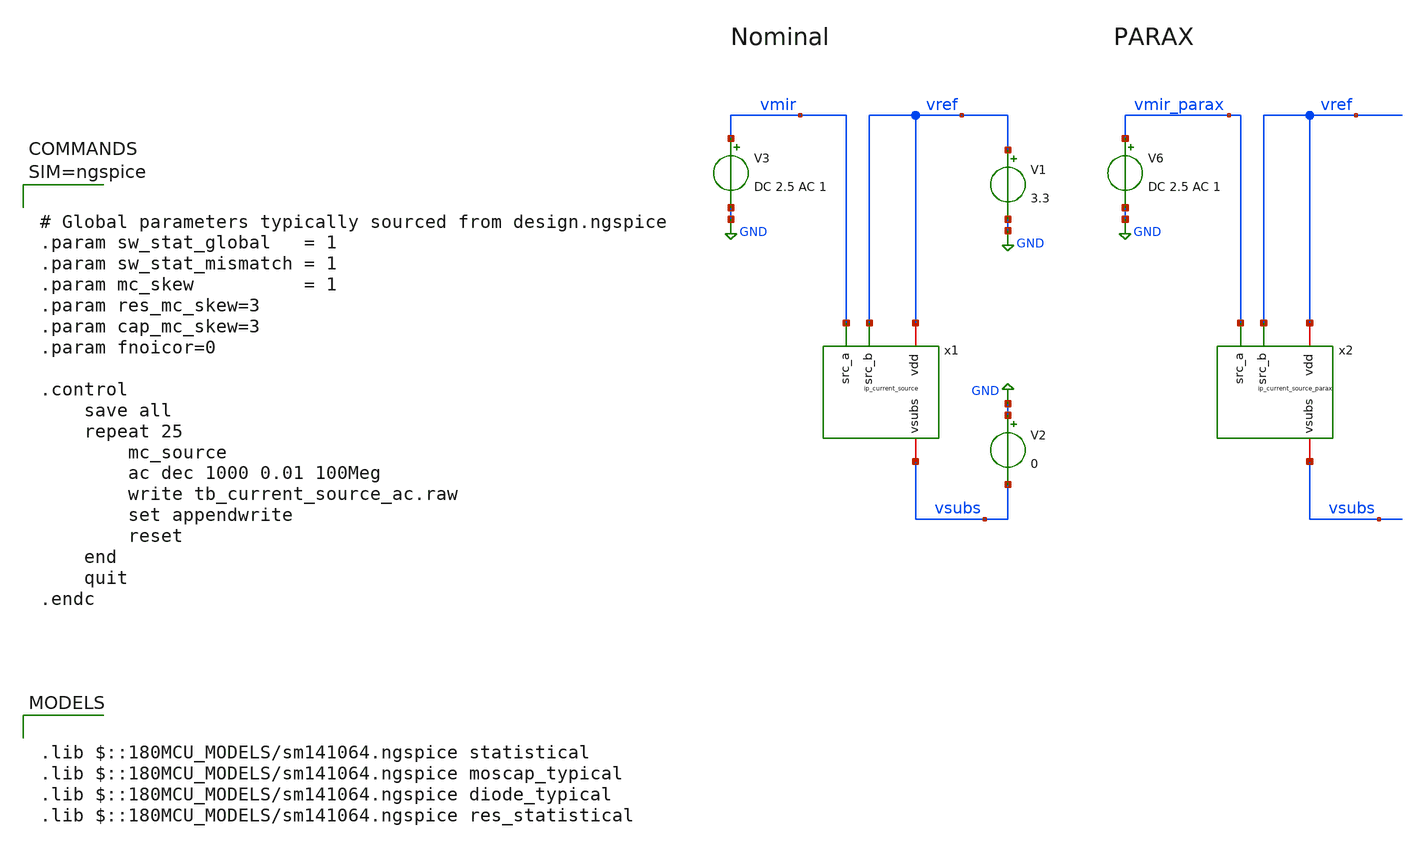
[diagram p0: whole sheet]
** sch_path: xschem/tb_current_source_ac.sch
**.subckt tb_current_source_ac
x1 vref vmir vsubs vref ip_current_source
V1 vref GND 3.3
V2 GND vsubs 0
V3 vmir GND DC 2.5 AC 1
x2 vref vmir_parax vsubs vref ip_current_source_parax
V6 vmir_parax GND DC 2.5 AC 1
**** begin user architecture code

.lib $::180MCU_MODELS/sm141064.ngspice statistical
.lib $::180MCU_MODELS/sm141064.ngspice moscap_typical
.lib $::180MCU_MODELS/sm141064.ngspice diode_typical
.lib $::180MCU_MODELS/sm141064.ngspice res_statistical




# Global parameters typically sourced from design.ngspice
.param sw_stat_global   = 1
.param sw_stat_mismatch = 1
.param mc_skew          = 1
.param res_mc_skew=3
.param cap_mc_skew=3
.param fnoicor=0

.control
	save all
	repeat 25
		mc_source
		ac dec 1000 0.01 100Meg
		write tb_current_source_ac.raw
		set appendwrite
		reset
	end
	quit
.endc



**** end user architecture code
**.ends

* expanding   symbol:  ip_current_source.sym # of pins=4
** sym_path: xschem/ip_current_source.sym
** sch_path: xschem/ip_current_source.sch
.subckt ip_current_source vdd src_a vsubs src_b
*.iopin vdd
*.iopin vsubs
*.ipin src_a
*.ipin src_b
XR1 refin net3 vsubs ppolyf_u_1k r_width=1e-6 r_length=6e-6 m=1
XR2 net3 net2 vsubs ppolyf_u_1k r_width=1e-6 r_length=6e-6 m=1
XR3 net2 net4 vsubs ppolyf_u_1k r_width=1e-6 r_length=6e-6 m=1
XR4 net4 net6 vsubs ppolyf_u_1k r_width=1e-6 r_length=6e-6 m=1
XR5 net6 net5 vsubs ppolyf_u_1k r_width=1e-6 r_length=6e-6 m=1
XR6 net5 vdd vsubs ppolyf_u_1k r_width=1e-6 r_length=6e-6 m=1
XM8 refin refin vsubs vsubs nfet_06v0 L=1u W=5u nf=1 ad='int((nf+1)/2) * W/nf * 0.18u' as='int((nf+2)/2) * W/nf * 0.18u'
+ pd='2*int((nf+1)/2) * (W/nf + 0.18u)' ps='2*int((nf+2)/2) * (W/nf + 0.18u)' nrd='0.18u / W' nrs='0.18u / W'
+ sa=0 sb=0 sd=0 m=1 par=1
XM5 src_a refin net1 vsubs nfet_06v0 L=0.7u W=5u nf=1 ad='int((nf+1)/2) * W/nf * 0.18u' as='int((nf+2)/2) * W/nf * 0.18u'
+ pd='2*int((nf+1)/2) * (W/nf + 0.18u)' ps='2*int((nf+2)/2) * (W/nf + 0.18u)' nrd='0.18u / W' nrs='0.18u / W'
+ sa=0 sb=0 sd=0 m=1 par=1
XM2 src_a refin net1 vsubs nfet_06v0 L=0.7u W=5u nf=1 ad='int((nf+1)/2) * W/nf * 0.18u' as='int((nf+2)/2) * W/nf * 0.18u'
+ pd='2*int((nf+1)/2) * (W/nf + 0.18u)' ps='2*int((nf+2)/2) * (W/nf + 0.18u)' nrd='0.18u / W' nrs='0.18u / W'
+ sa=0 sb=0 sd=0 m=1 par=1
XM3 src_b refin net7 vsubs nfet_06v0 L=0.7u W=5u nf=1 ad='int((nf+1)/2) * W/nf * 0.18u' as='int((nf+2)/2) * W/nf * 0.18u'
+ pd='2*int((nf+1)/2) * (W/nf + 0.18u)' ps='2*int((nf+2)/2) * (W/nf + 0.18u)' nrd='0.18u / W' nrs='0.18u / W'
+ sa=0 sb=0 sd=0 m=1 par=1
XM6 src_b refin net7 vsubs nfet_06v0 L=0.7u W=5u nf=1 ad='int((nf+1)/2) * W/nf * 0.18u' as='int((nf+2)/2) * W/nf * 0.18u'
+ pd='2*int((nf+1)/2) * (W/nf + 0.18u)' ps='2*int((nf+2)/2) * (W/nf + 0.18u)' nrd='0.18u / W' nrs='0.18u / W'
+ sa=0 sb=0 sd=0 m=1 par=1
XM4 net1 refin vsubs vsubs nfet_06v0 L=5u W=0.5u nf=1 ad='int((nf+1)/2) * W/nf * 0.18u' as='int((nf+2)/2) * W/nf * 0.18u'
+ pd='2*int((nf+1)/2) * (W/nf + 0.18u)' ps='2*int((nf+2)/2) * (W/nf + 0.18u)' nrd='0.18u / W' nrs='0.18u / W'
+ sa=0 sb=0 sd=0 m=1 par=1
XM7 net7 refin vsubs vsubs nfet_06v0 L=5u W=0.5u nf=1 ad='int((nf+1)/2) * W/nf * 0.18u' as='int((nf+2)/2) * W/nf * 0.18u'
+ pd='2*int((nf+1)/2) * (W/nf + 0.18u)' ps='2*int((nf+2)/2) * (W/nf + 0.18u)' nrd='0.18u / W' nrs='0.18u / W'
+ sa=0 sb=0 sd=0 m=1 par=1
.ends


* expanding   symbol:  ip_current_source_parax.sym # of pins=4
** sym_path: xschem/ip_current_source.sym
.include [file normalize ../mag/ip_current_source.sim.spice]
.GLOBAL GND
.end
